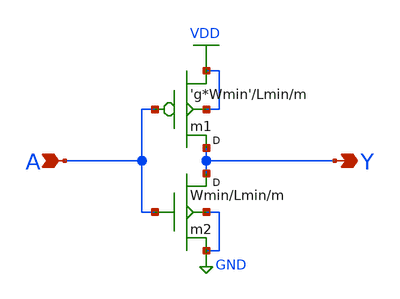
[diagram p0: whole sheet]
** sch_path: Sources/crafted/inv.sch
**.subckt inv A Y
*.ipin A
*.opin Y
m2 Y A GND GND nmos4 w=Wmin l=Lmin m=m
m1 Y A VDD VDD pmos4 w='g*Wmin' l=Lmin m=m
**.ends
.GLOBAL VDD
.GLOBAL GND
.end
